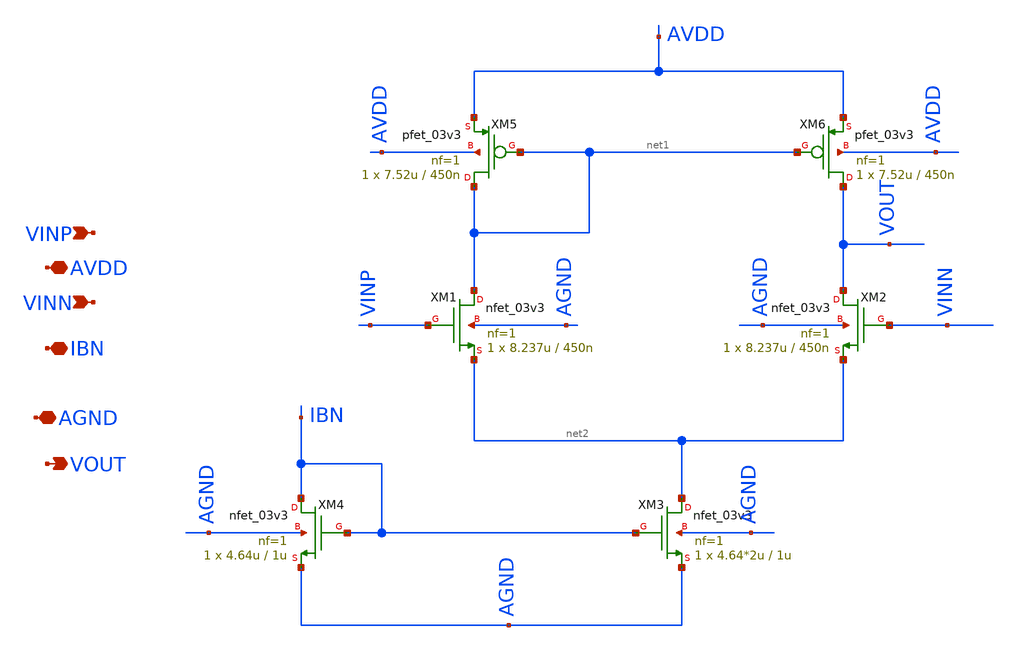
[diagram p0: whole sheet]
** sch_path: Lab_07/OTA_sch.sch
**.subckt OTA_sch AVDD IBN AGND VOUT VINN VINP
*.iopin AVDD
*.iopin IBN
*.iopin AGND
*.opin VOUT
*.ipin VINN
*.ipin VINP
XM1 net1 VINP net2 AGND nfet_03v3 L=450n W=8.237u nf=1 ad='int((nf+1)/2) * W/nf * 0.18u' as='int((nf+2)/2) * W/nf * 0.18u'
+ pd='2*int((nf+1)/2) * (W/nf + 0.18u)' ps='2*int((nf+2)/2) * (W/nf + 0.18u)' nrd='0.18u / W' nrs='0.18u / W'
+ sa=0 sb=0 sd=0 m=1
XM2 VOUT VINN net2 AGND nfet_03v3 L=450n W=8.237u nf=1 ad='int((nf+1)/2) * W/nf * 0.18u' as='int((nf+2)/2) * W/nf * 0.18u'
+ pd='2*int((nf+1)/2) * (W/nf + 0.18u)' ps='2*int((nf+2)/2) * (W/nf + 0.18u)' nrd='0.18u / W' nrs='0.18u / W'
+ sa=0 sb=0 sd=0 m=1
XM3 net2 IBN AGND AGND nfet_03v3 L=1u W=4.64*2u nf=1 ad='int((nf+1)/2) * W/nf * 0.18u' as='int((nf+2)/2) * W/nf * 0.18u'
+ pd='2*int((nf+1)/2) * (W/nf + 0.18u)' ps='2*int((nf+2)/2) * (W/nf + 0.18u)' nrd='0.18u / W' nrs='0.18u / W'
+ sa=0 sb=0 sd=0 m=1
XM4 IBN IBN AGND AGND nfet_03v3 L=1u W=4.64u nf=1 ad='int((nf+1)/2) * W/nf * 0.18u' as='int((nf+2)/2) * W/nf * 0.18u'
+ pd='2*int((nf+1)/2) * (W/nf + 0.18u)' ps='2*int((nf+2)/2) * (W/nf + 0.18u)' nrd='0.18u / W' nrs='0.18u / W'
+ sa=0 sb=0 sd=0 m=1
XM5 net1 net1 AVDD AVDD pfet_03v3 L=450n W=7.52u nf=1 ad='int((nf+1)/2) * W/nf * 0.18u' as='int((nf+2)/2) * W/nf * 0.18u'
+ pd='2*int((nf+1)/2) * (W/nf + 0.18u)' ps='2*int((nf+2)/2) * (W/nf + 0.18u)' nrd='0.18u / W' nrs='0.18u / W'
+ sa=0 sb=0 sd=0 m=1
XM6 VOUT net1 AVDD AVDD pfet_03v3 L=450n W=7.52u nf=1 ad='int((nf+1)/2) * W/nf * 0.18u' as='int((nf+2)/2) * W/nf * 0.18u'
+ pd='2*int((nf+1)/2) * (W/nf + 0.18u)' ps='2*int((nf+2)/2) * (W/nf + 0.18u)' nrd='0.18u / W' nrs='0.18u / W'
+ sa=0 sb=0 sd=0 m=1
**.ends
.end
